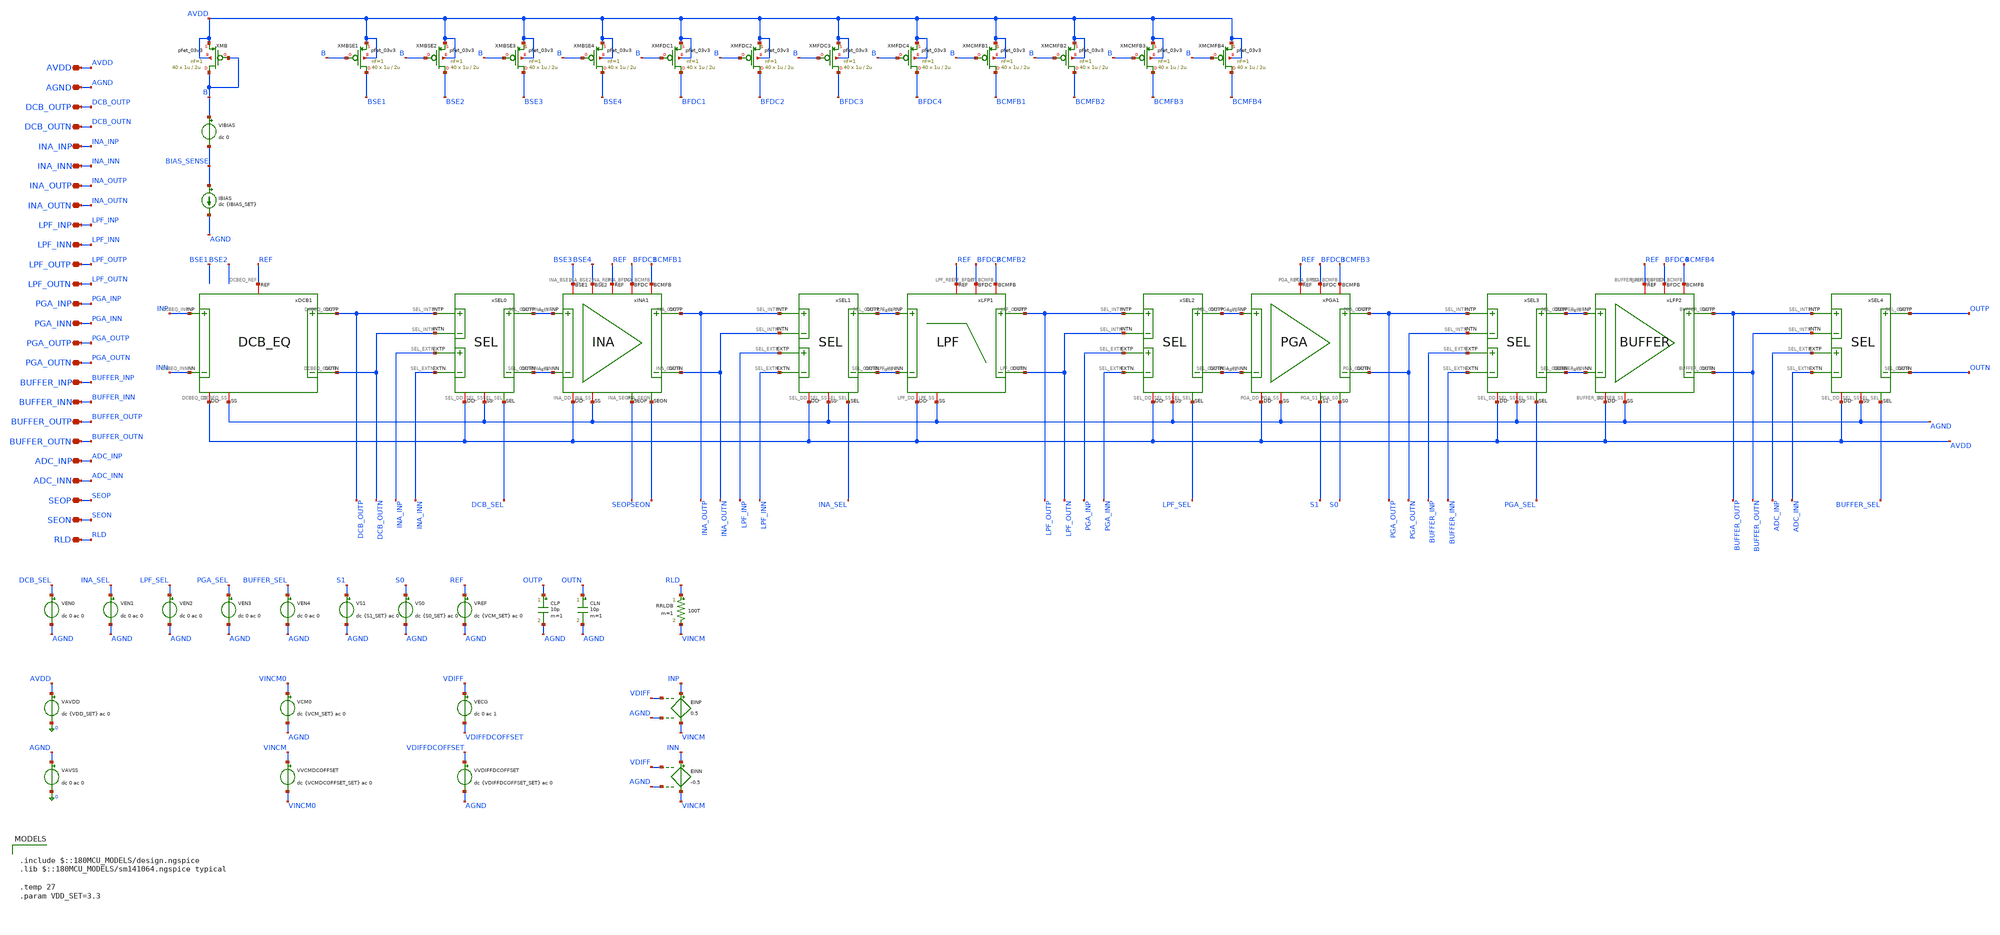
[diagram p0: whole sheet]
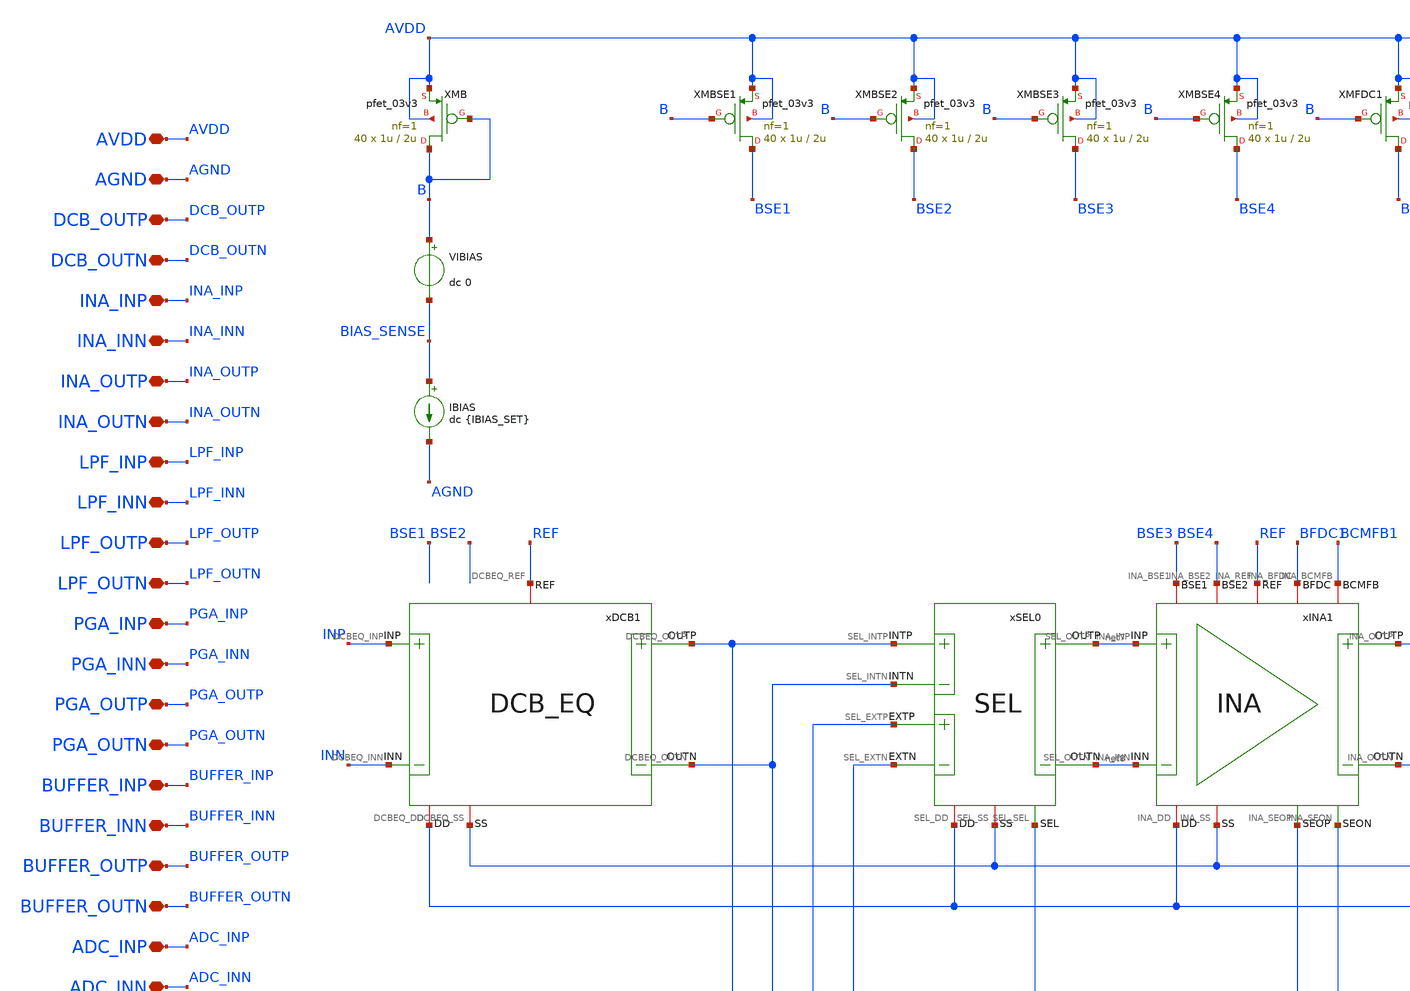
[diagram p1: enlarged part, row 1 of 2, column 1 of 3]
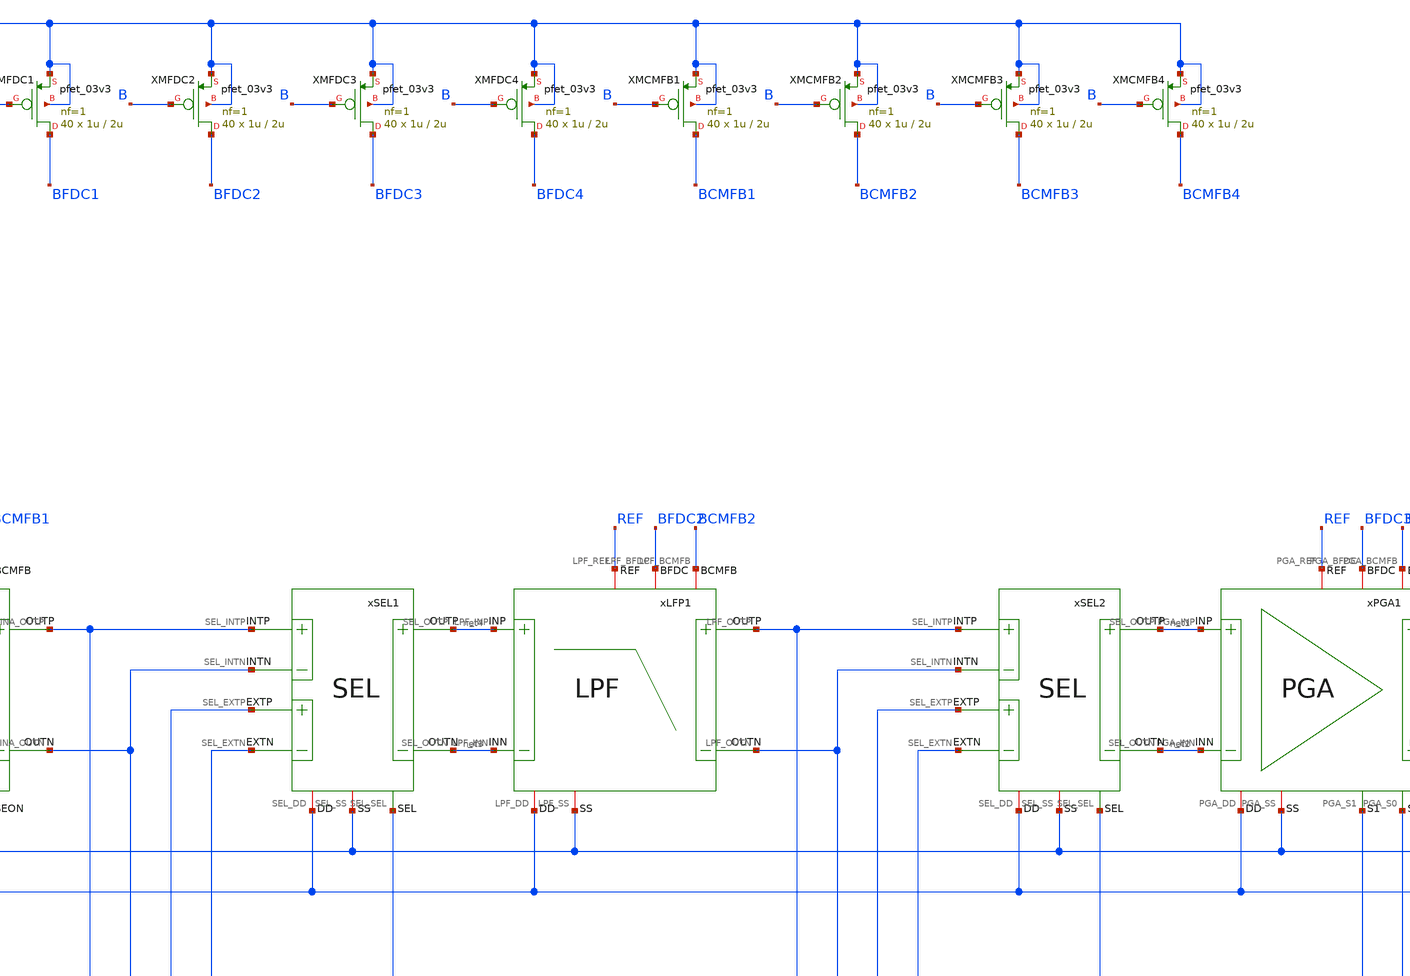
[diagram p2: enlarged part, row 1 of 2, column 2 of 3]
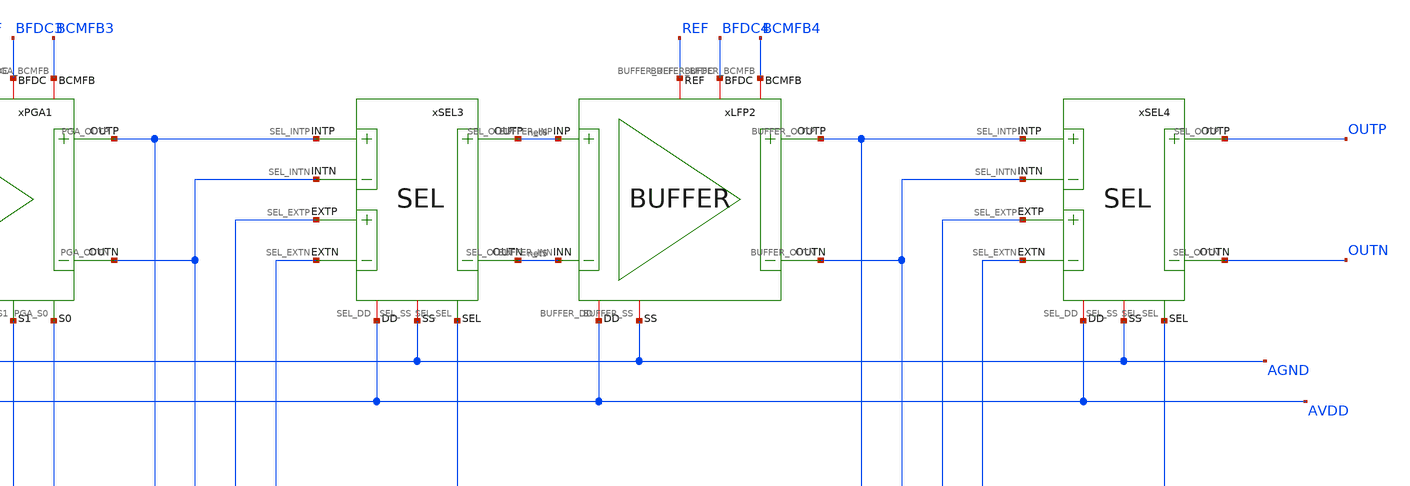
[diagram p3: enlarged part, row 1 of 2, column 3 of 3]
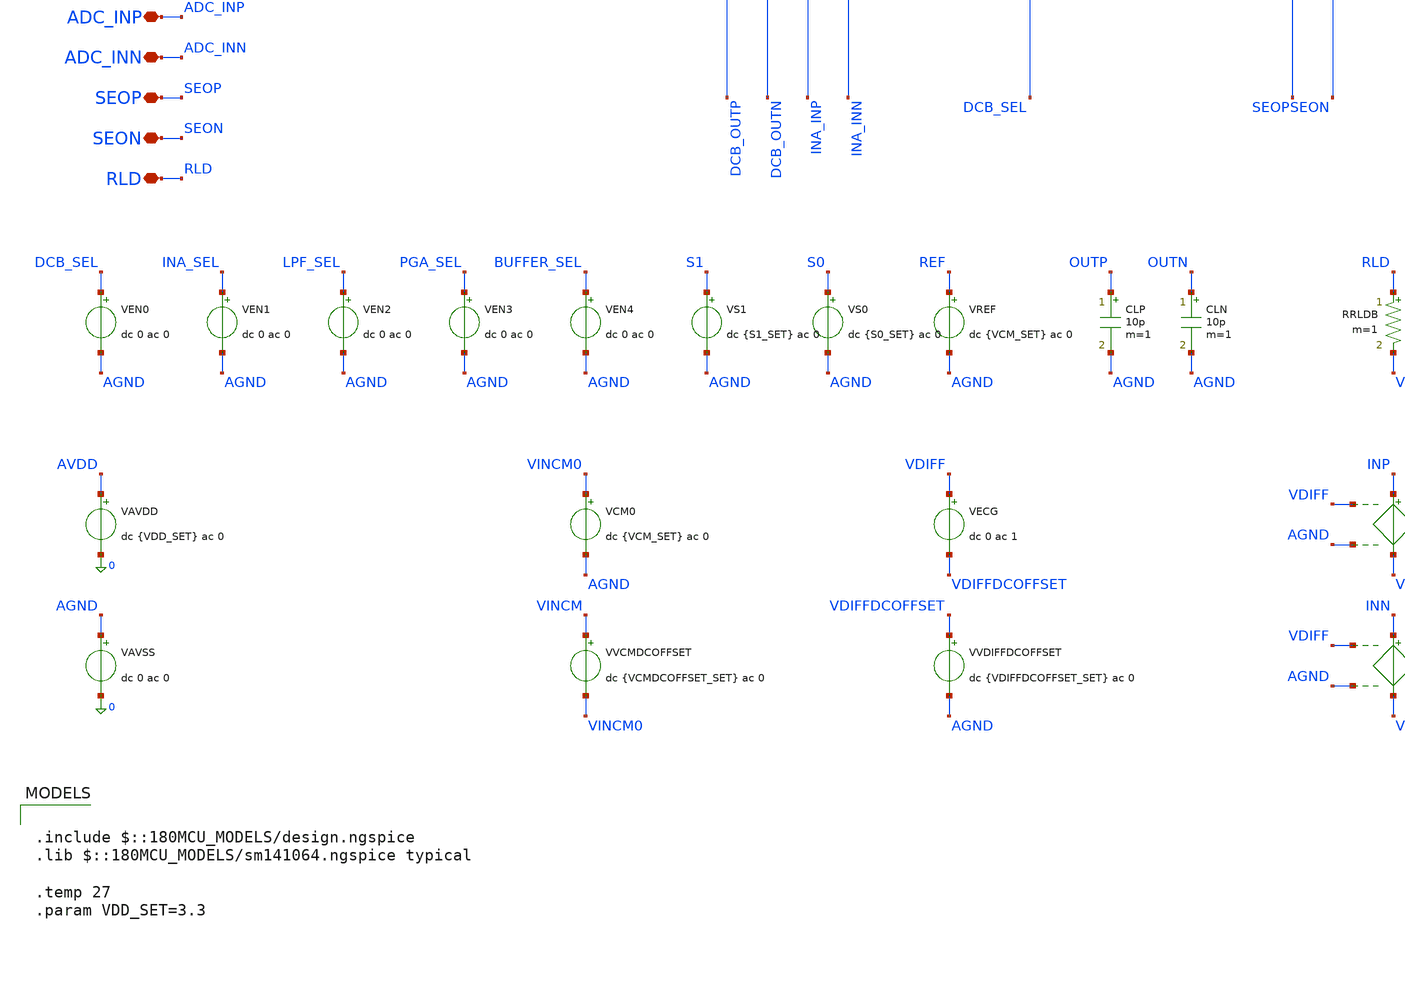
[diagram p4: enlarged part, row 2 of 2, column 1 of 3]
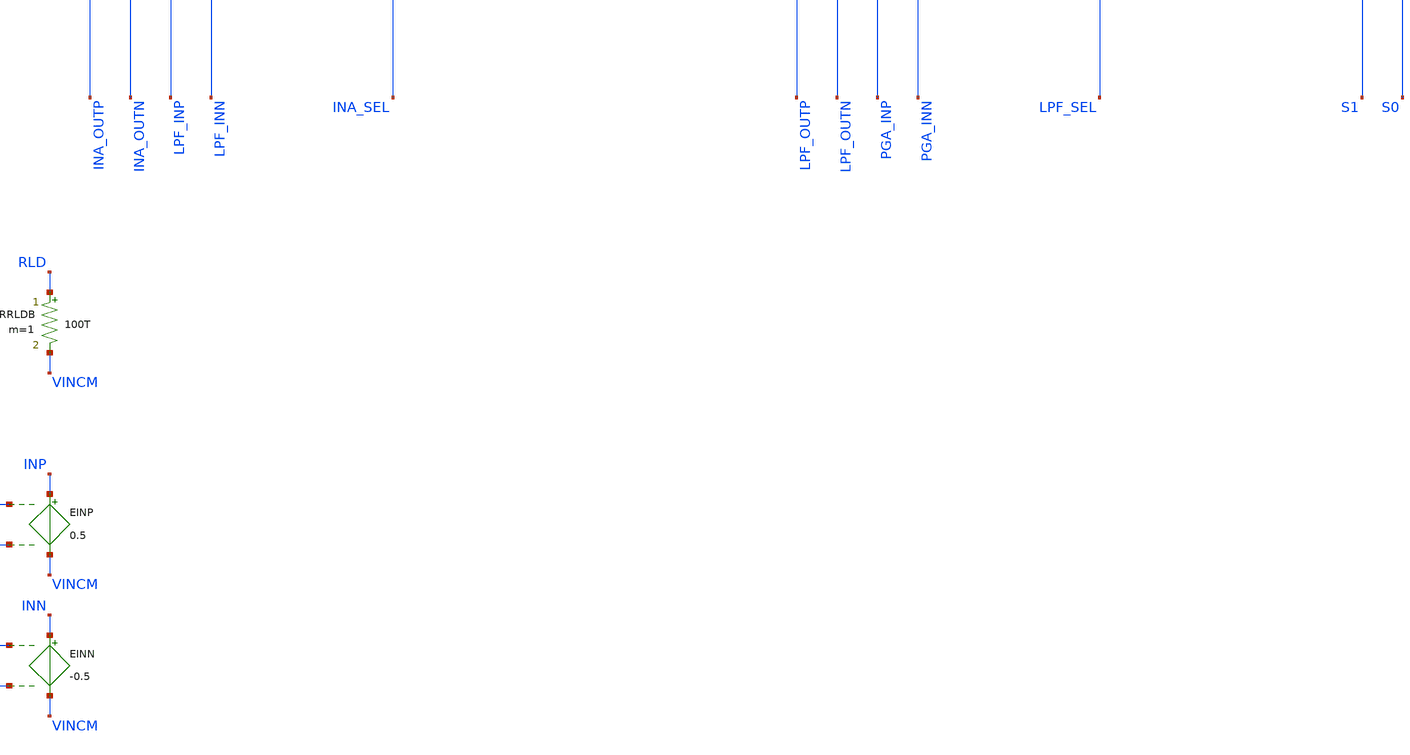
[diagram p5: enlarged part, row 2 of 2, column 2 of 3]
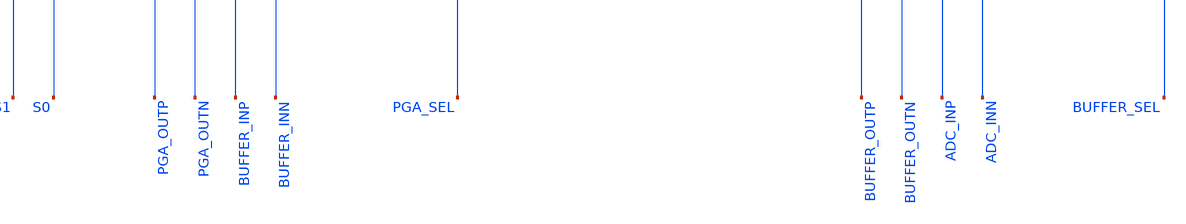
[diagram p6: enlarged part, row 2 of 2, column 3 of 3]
** sch_path: Design_Files/IC Design/Testbench/PATH/NOISE/PATH_TB_NOISE.sch
**.subckt PATH_TB_NOISE DCB_OUTP DCB_OUTN INA_INP INA_INN INA_OUTP INA_OUTN LPF_INP LPF_INN LPF_OUTP
*+ LPF_OUTN PGA_INP PGA_INN PGA_OUTP PGA_OUTN BUFFER_INP BUFFER_INN BUFFER_OUTP BUFFER_OUTN ADC_INP ADC_INN
*+ AVDD AGND SEOP SEON RLD
*.iopin DCB_OUTP
*.iopin DCB_OUTN
*.iopin INA_INP
*.iopin INA_INN
*.iopin INA_OUTP
*.iopin INA_OUTN
*.iopin LPF_INP
*.iopin LPF_INN
*.iopin LPF_OUTP
*.iopin LPF_OUTN
*.iopin PGA_INP
*.iopin PGA_INN
*.iopin PGA_OUTP
*.iopin PGA_OUTN
*.iopin BUFFER_INP
*.iopin BUFFER_INN
*.iopin BUFFER_OUTP
*.iopin BUFFER_OUTN
*.iopin ADC_INP
*.iopin ADC_INN
*.iopin AVDD
*.iopin AGND
*.iopin SEOP
*.iopin SEON
*.iopin RLD
CLP OUTP AGND 10p m=1
CLN OUTN AGND 10p m=1
VIBIAS B BIAS_SENSE dc 0
.save i(vibias)
IBIAS BIAS_SENSE AGND dc {IBIAS_SET}
VREF REF AGND dc {VCM_SET} ac 0
xLFP1 AVDD AGND net4 net3 LPF_OUTN BFDC2 LPF_OUTP BCMFB2 REF LPF
xPGA1 AVDD AGND net1 net2 PGA_OUTN BFDC3 PGA_OUTP BCMFB3 REF S1 S0 PGA
xSEL1 AVDD AGND INA_OUTP INA_OUTN net3 net4 LPF_INP LPF_INN INA_SEL SEL
xINA1 AVDD AGND net7 net8 INA_OUTN BFDC1 INA_OUTP BCMFB1 REF SEON SEOP BSE3 BSE4 INA
xSEL2 AVDD AGND LPF_OUTP LPF_OUTN net2 net1 PGA_INP PGA_INN LPF_SEL SEL
xSEL3 AVDD AGND PGA_OUTP PGA_OUTN net5 net6 BUFFER_INP BUFFER_INN PGA_SEL SEL
xSEL4 AVDD AGND BUFFER_OUTP BUFFER_OUTN OUTN OUTP ADC_INP ADC_INN BUFFER_SEL SEL
xLFP2 AVDD AGND net6 net5 BUFFER_OUTN BFDC4 BUFFER_OUTP BCMFB4 REF BUFFER
VEN1 INA_SEL AGND dc 0 ac 0
.save i(ven1)
VS0 S0 AGND dc {S0_SET} ac 0
VS1 S1 AGND dc {S1_SET} ac 0
xSEL0 AVDD AGND DCB_OUTP DCB_OUTN net8 net7 INA_INP INA_INN DCB_SEL SEL
VEN2 LPF_SEL AGND dc 0 ac 0
.save i(ven2)
VEN3 PGA_SEL AGND dc 0 ac 0
.save i(ven3)
VEN4 BUFFER_SEL AGND dc 0 ac 0
.save i(ven4)
VEN0 DCB_SEL AGND dc 0 ac 0
.save i(ven0)
xDCB1 AVDD AGND INP INN DCB_OUTP DCB_OUTN REF DCB_EQ
VAVDD AVDD 0 dc {VDD_SET} ac 0
.save i(vavdd)
VAVSS AGND 0 dc 0 ac 0
.save i(vavss)
VCM0 VINCM0 AGND dc {VCM_SET} ac 0
VVCMDCOFFSET VINCM VINCM0 dc {VCMDCOFFSET_SET} ac 0
VECG VDIFF VDIFFDCOFFSET dc 0 ac 1
VVDIFFDCOFFSET VDIFFDCOFFSET AGND dc {VDIFFDCOFFSET_SET} ac 0
EINP INP VINCM VDIFF AGND 0.5
EINN INN VINCM VDIFF AGND -0.5
RRLDB RLD VINCM 100T m=1
XMB B B AVDD AVDD pfet_03v3 L=2u W=1u nf=1 ad='int((nf+1)/2) * W/nf * 0.18u' as='int((nf+2)/2) * W/nf * 0.18u'
+ pd='2*int((nf+1)/2) * (W/nf + 0.18u)' ps='2*int((nf+2)/2) * (W/nf + 0.18u)' nrd='0.18u / W' nrs='0.18u / W'
+ sa=0 sb=0 sd=0 m=40
XMBSE3 BSE3 B AVDD AVDD pfet_03v3 L=2u W=1u nf=1 ad='int((nf+1)/2) * W/nf * 0.18u' as='int((nf+2)/2) * W/nf * 0.18u'
+ pd='2*int((nf+1)/2) * (W/nf + 0.18u)' ps='2*int((nf+2)/2) * (W/nf + 0.18u)' nrd='0.18u / W' nrs='0.18u / W'
+ sa=0 sb=0 sd=0 m=40
XMBSE4 BSE4 B AVDD AVDD pfet_03v3 L=2u W=1u nf=1 ad='int((nf+1)/2) * W/nf * 0.18u' as='int((nf+2)/2) * W/nf * 0.18u'
+ pd='2*int((nf+1)/2) * (W/nf + 0.18u)' ps='2*int((nf+2)/2) * (W/nf + 0.18u)' nrd='0.18u / W' nrs='0.18u / W'
+ sa=0 sb=0 sd=0 m=40
XMFDC1 BFDC1 B AVDD AVDD pfet_03v3 L=2u W=1u nf=1 ad='int((nf+1)/2) * W/nf * 0.18u' as='int((nf+2)/2) * W/nf * 0.18u'
+ pd='2*int((nf+1)/2) * (W/nf + 0.18u)' ps='2*int((nf+2)/2) * (W/nf + 0.18u)' nrd='0.18u / W' nrs='0.18u / W'
+ sa=0 sb=0 sd=0 m=40
XMFDC2 BFDC2 B AVDD AVDD pfet_03v3 L=2u W=1u nf=1 ad='int((nf+1)/2) * W/nf * 0.18u' as='int((nf+2)/2) * W/nf * 0.18u'
+ pd='2*int((nf+1)/2) * (W/nf + 0.18u)' ps='2*int((nf+2)/2) * (W/nf + 0.18u)' nrd='0.18u / W' nrs='0.18u / W'
+ sa=0 sb=0 sd=0 m=40
XMFDC3 BFDC3 B AVDD AVDD pfet_03v3 L=2u W=1u nf=1 ad='int((nf+1)/2) * W/nf * 0.18u' as='int((nf+2)/2) * W/nf * 0.18u'
+ pd='2*int((nf+1)/2) * (W/nf + 0.18u)' ps='2*int((nf+2)/2) * (W/nf + 0.18u)' nrd='0.18u / W' nrs='0.18u / W'
+ sa=0 sb=0 sd=0 m=40
XMFDC4 BFDC4 B AVDD AVDD pfet_03v3 L=2u W=1u nf=1 ad='int((nf+1)/2) * W/nf * 0.18u' as='int((nf+2)/2) * W/nf * 0.18u'
+ pd='2*int((nf+1)/2) * (W/nf + 0.18u)' ps='2*int((nf+2)/2) * (W/nf + 0.18u)' nrd='0.18u / W' nrs='0.18u / W'
+ sa=0 sb=0 sd=0 m=40
XMCMFB1 BCMFB1 B AVDD AVDD pfet_03v3 L=2u W=1u nf=1 ad='int((nf+1)/2) * W/nf * 0.18u' as='int((nf+2)/2) * W/nf * 0.18u'
+ pd='2*int((nf+1)/2) * (W/nf + 0.18u)' ps='2*int((nf+2)/2) * (W/nf + 0.18u)' nrd='0.18u / W' nrs='0.18u / W'
+ sa=0 sb=0 sd=0 m=40
XMCMFB2 BCMFB2 B AVDD AVDD pfet_03v3 L=2u W=1u nf=1 ad='int((nf+1)/2) * W/nf * 0.18u' as='int((nf+2)/2) * W/nf * 0.18u'
+ pd='2*int((nf+1)/2) * (W/nf + 0.18u)' ps='2*int((nf+2)/2) * (W/nf + 0.18u)' nrd='0.18u / W' nrs='0.18u / W'
+ sa=0 sb=0 sd=0 m=40
XMCMFB3 BCMFB3 B AVDD AVDD pfet_03v3 L=2u W=1u nf=1 ad='int((nf+1)/2) * W/nf * 0.18u' as='int((nf+2)/2) * W/nf * 0.18u'
+ pd='2*int((nf+1)/2) * (W/nf + 0.18u)' ps='2*int((nf+2)/2) * (W/nf + 0.18u)' nrd='0.18u / W' nrs='0.18u / W'
+ sa=0 sb=0 sd=0 m=40
XMCMFB4 BCMFB4 B AVDD AVDD pfet_03v3 L=2u W=1u nf=1 ad='int((nf+1)/2) * W/nf * 0.18u' as='int((nf+2)/2) * W/nf * 0.18u'
+ pd='2*int((nf+1)/2) * (W/nf + 0.18u)' ps='2*int((nf+2)/2) * (W/nf + 0.18u)' nrd='0.18u / W' nrs='0.18u / W'
+ sa=0 sb=0 sd=0 m=40
XMBSE1 BSE1 B AVDD AVDD pfet_03v3 L=2u W=1u nf=1 ad='int((nf+1)/2) * W/nf * 0.18u' as='int((nf+2)/2) * W/nf * 0.18u'
+ pd='2*int((nf+1)/2) * (W/nf + 0.18u)' ps='2*int((nf+2)/2) * (W/nf + 0.18u)' nrd='0.18u / W' nrs='0.18u / W'
+ sa=0 sb=0 sd=0 m=40
XMBSE2 BSE2 B AVDD AVDD pfet_03v3 L=2u W=1u nf=1 ad='int((nf+1)/2) * W/nf * 0.18u' as='int((nf+2)/2) * W/nf * 0.18u'
+ pd='2*int((nf+1)/2) * (W/nf + 0.18u)' ps='2*int((nf+2)/2) * (W/nf + 0.18u)' nrd='0.18u / W' nrs='0.18u / W'
+ sa=0 sb=0 sd=0 m=40
**** begin user architecture code

.include $::180MCU_MODELS/design.ngspice
.lib $::180MCU_MODELS/sm141064.ngspice typical

.temp 27
.param VDD_SET=3.3



.param VCM_SET={VDD_SET/2}

.param VCMDCOFFSET_SET=0
.param VDIFFDCOFFSET_SET=0

.param IBIAS_SET=40u

.param S1_SET=3.3
.param S0_SET=3.3

.options sparse
.options method=gear

.options reltol=1e-3
.options abstol=1e-12
.options vntol=1u
.options chgtol=1e-14

.options itl1=2000
.options itl2=1000
.options itl4=2000

.options gmin=1e-12
.options rshunt=100T

.nodeset v(B)=2.3

.nodeset v(INP)={VCM_SET}
.nodeset v(INN)={VCM_SET}

.nodeset v(OUTP)={VCM_SET}
.nodeset v(OUTN)={VCM_SET}

.nodeset v(RLD)={VCM_SET}

.save all





.control

destroy all

set noaskquit
set wr_singlescale
unset wr_vecnames
set appendwrite

unset sqrnoise

option numdgt=15
option sparse

shell mkdir -p
+ /foss/designs/ECG_Acquisition_IC/Measurement_Results/IC_Simulation/PATH/NOM.Result_txt

shell rm -f
+ /foss/designs/ECG_Acquisition_IC/Measurement_Results/IC_Simulation/PATH/NOM.Result_txt/NOM.noise_diff.txt


* Differential noise: PGA G2 and G16
foreach gaincfg 0 1

    if $gaincfg = 0
        alterparam S1_SET=0
        alterparam S0_SET=0
    else
        alterparam S1_SET=3.3
        alterparam S0_SET=3.3
    end

    reset
    save all

    alter @VECG[ACMAG]=1
    alter @VECG[ACPHASE]=0

    alter @VCM0[ACMAG]=0
    alter @VCM0[ACPHASE]=0

    alter @VAVDD[ACMAG]=0
    alter @VAVDD[ACPHASE]=0

    alter @VAVSS[ACMAG]=0
    alter @VAVSS[ACPHASE]=0

    op

    noise v(OUTP,OUTN) VECG dec 300 0.01 1k

    * noise leaves the one-row integrated plot active
    * previous plot contains the noise-density spectrum
    setplot previous
    setscale frequency

    if $gaincfg = 0
        let noise_pga_gain=frequency*0+2
    else
        let noise_pga_gain=frequency*0+16
    end

    let noise_out_density=onoise_spectrum
    let noise_in_density=inoise_spectrum

    wrdata
+ /foss/designs/ECG_Acquisition_IC/Measurement_Results/IC_Simulation/PATH/NOM.Result_txt/NOM.noise_diff.txt noise_pga_gain noise_out_density noise_in_density

    destroy all

end


* Last simulated setting is PGA G16

quit
.endc


**** end user architecture code
**.ends

* expanding   symbol:  ECG_Acquisition_IC/Design_Files/IC Design/Schematic/LPF/LPF.sym # of pins=9
** sym_path: Design_Files/IC Design/Schematic/LPF/LPF.sym
** sch_path: Design_Files/IC Design/Schematic/LPF/LPF.sch
.subckt LPF LPF_DD LPF_SS LPF_INP LPF_INN LPF_OUTN LPF_BFDC LPF_OUTP LPF_BCMFB LPF_REF
*.iopin LPF_DD
*.iopin LPF_SS
*.ipin LPF_INP
*.ipin LPF_INN
*.opin LPF_OUTP
*.iopin LPF_BFDC
*.opin LPF_OUTN
*.iopin LPF_BCMFB
*.iopin LPF_REF
RFBP net1 LPF_OUTN 3.7Meg m=1
xFDOTA1 LPF_DD LPF_SS net1 net2 LPF_OUTN LPF_BFDC LPF_OUTP LPF_BCMFB LPF_REF LPF_VOCM FD_OTA
RINN LPF_INN net2 3.7Meg m=1
RINP LPF_INP net1 3.7Meg m=1
RFBN net2 LPF_OUTP 3.7Meg m=1
CLPFP net1 LPF_OUTN 20p m=5
CLPFN net2 LPF_OUTP 20p m=5
.ends


* expanding   symbol:  ECG_Acquisition_IC/Design_Files/IC Design/Schematic/PGA/PGA.sym # of pins=11
** sym_path: Design_Files/IC Design/Schematic/PGA/PGA.sym
** sch_path: Design_Files/IC Design/Schematic/PGA/PGA.sch
.subckt PGA PGA_DD PGA_SS PGA_INP PGA_INN PGA_OUTN PGA_BFDC PGA_OUTP PGA_BCMFB PGA_REF PGA_S1 PGA_S0
*.iopin PGA_DD
*.iopin PGA_SS
*.ipin PGA_INP
*.ipin PGA_INN
*.opin PGA_OUTP
*.iopin PGA_BFDC
*.opin PGA_OUTN
*.iopin PGA_BCMFB
*.iopin PGA_REF
*.ipin PGA_S0
*.ipin PGA_S1
RFBP1 net2 net1 40k m=1
xFDOTA1 PGA_DD PGA_SS net2 net8 PGA_OUTN PGA_BFDC PGA_OUTP PGA_BCMFB PGA_REF PGA_VOCM FD_OTA
RFBP2 net1 net3 40k m=1
RFBP3 net3 net4 120k m=1
RFBP4 net4 PGA_OUTN 120k m=1
RINN PGA_INN net8 20k m=1
RINP PGA_INP net2 20k m=1
xTG1 PGA_DD PGA_SS net1 net3 S0B PGA_S0 TG
xTG3 PGA_DD PGA_SS net3 PGA_OUTN S1B PGA_S1 TG
xINV1 PGA_DD PGA_SS PGA_S0 S0B INV
xTG2 PGA_DD PGA_SS net3 net4 S0B PGA_S0 TG
RFBN1 net8 net5 40k m=1
RFBN2 net5 net6 40k m=1
RFBN3 net6 net7 120k m=1
RFBN4 net7 PGA_OUTP 120k m=1
xTG4 PGA_DD PGA_SS net5 net6 S0B PGA_S0 TG
xTG5 PGA_DD PGA_SS net6 net7 S0B PGA_S0 TG
xINV2 PGA_DD PGA_SS PGA_S1 S1B INV
xTG6 PGA_DD PGA_SS net6 PGA_OUTP S1B PGA_S1 TG
.ends


* expanding   symbol:  ECG_Acquisition_IC/Design_Files/IC Design/Schematic/SEL/SEL.sym # of pins=9
** sym_path: Design_Files/IC Design/Schematic/SEL/SEL.sym
** sch_path: Design_Files/IC Design/Schematic/SEL/SEL.sch
.subckt SEL SEL_DD SEL_SS SEL_INTP SEL_INTN SEL_OUTN SEL_OUTP SEL_EXTP SEL_EXTN SEL_SEL
*.iopin SEL_DD
*.iopin SEL_SS
*.ipin SEL_INTP
*.ipin SEL_INTN
*.iopin SEL_OUTP
*.iopin SEL_OUTN
*.ipin SEL_EXTP
*.ipin SEL_EXTN
*.ipin SEL_SEL
xINV1 SEL_DD SEL_SS SEL_SEL SELB INV
xTG1 SEL_DD SEL_SS SEL_EXTP SEL_OUTP SEL_SEL SELB TG
xTG2 SEL_DD SEL_SS SEL_INTP SEL_OUTP SELB SEL_SEL TG
xTG3 SEL_DD SEL_SS SEL_EXTN SEL_OUTN SEL_SEL SELB TG
xTG4 SEL_DD SEL_SS SEL_INTN SEL_OUTN SELB SEL_SEL TG
.ends


* expanding   symbol:  ECG_Acquisition_IC/Design_Files/IC Design/Schematic/INA/INA.sym # of pins=13
** sym_path: Design_Files/IC Design/Schematic/INA/INA.sym
** sch_path: Design_Files/IC Design/Schematic/INA/INA.sch
.subckt INA INA_DD INA_SS INA_INP INA_INN INA_OUTN INA_BFDC INA_OUTP INA_BCMFB INA_REF INA_SEON
+ INA_SEOP INA_BSE1 INA_BSE2
*.iopin INA_DD
*.iopin INA_SS
*.ipin INA_INP
*.ipin INA_INN
*.opin INA_OUTP
*.iopin INA_BFDC
*.opin INA_OUTN
*.iopin INA_BCMFB
*.iopin INA_REF
*.iopin INA_BSE1
*.iopin INA_SEON
*.iopin INA_SEOP
*.iopin INA_BSE2
RFDFBP INA_FDINP INA_OUTN 40k m=1
xFDOTA1 INA_DD INA_SS INA_FDINP INA_FDINN INA_OUTN INA_BFDC INA_OUTP INA_BCMFB INA_REF INA_VOCM
+ FD_OTA
xSEOTA1 INA_DD INA_SS INA_INP INA_SEFP INA_SEOP INA_BSE1 SE_OTA
xSEOTA2 INA_DD INA_SS INA_INN INA_SEFN INA_SEON INA_BSE2 SE_OTA
RFDFBN INA_FDINN INA_OUTP 40k m=1
RFDINP INA_SEOP INA_FDINP 10k m=1
RFDINN INA_SEON INA_FDINN 10k m=1
RSEFP INA_SEOP INA_SEFP 118k m=1
RSEFN INA_SEON INA_SEFN 118k m=1
RSEG INA_SEFP INA_SEFN 4k m=1
.ends


* expanding   symbol:  ECG_Acquisition_IC/Design_Files/IC Design/Schematic/BUFFER/BUFFER.sym # of
*+ pins=9
** sym_path: Design_Files/IC Design/Schematic/BUFFER/BUFFER.sym
** sch_path: Design_Files/IC Design/Schematic/BUFFER/BUFFER.sch
.subckt BUFFER BUFFER_DD BUFFER_SS BUFFER_INP BUFFER_INN BUFFER_OUTN BUFFER_BFDC BUFFER_OUTP
+ BUFFER_BCMFB BUFFER_REF
*.iopin BUFFER_DD
*.iopin BUFFER_SS
*.ipin BUFFER_INP
*.ipin BUFFER_INN
*.opin BUFFER_OUTP
*.iopin BUFFER_BFDC
*.opin BUFFER_OUTN
*.iopin BUFFER_BCMFB
*.iopin BUFFER_REF
RFBP net1 BUFFER_OUTN 20k m=1
xFDOTA1 BUFFER_DD BUFFER_SS net1 net2 BUFFER_OUTN BUFFER_BFDC BUFFER_OUTP BUFFER_BCMFB BUFFER_REF
+ BUFFER_VOCM FD_OTA
RINN BUFFER_INN net2 20k m=1
RINP BUFFER_INP net1 20k m=1
RFBN net2 BUFFER_OUTP 20k m=1
.ends


* expanding   symbol:  ECG_Acquisition_IC/Design_Files/IC Design/Schematic/DCB_EQ/DCB_EQ.sym # of
*+ pins=7
** sym_path: Design_Files/IC Design/Schematic/DCB_EQ/DCB_EQ.sym
** sch_path: Design_Files/IC Design/Schematic/DCB_EQ/DCB_EQ.sch
.subckt DCB_EQ DCBEQ_DD DCBEQ_SS DCBEQ_INP DCBEQ_INN DCBEQ_OUTP DCBEQ_OUTN DCBEQ_REF
*.iopin DCBEQ_DD
*.iopin DCBEQ_SS
*.ipin DCBEQ_INP
*.ipin DCBEQ_INN
*.opin DCBEQ_OUTP
*.opin DCBEQ_OUTN
*.iopin DCBEQ_REF
CBP DCBEQ_INP DCBEQ_OUTP 20p m=25
CBN DCBEQ_INN DCBEQ_OUTN 20p m=25
REQP DCBEQ_OUTP DCBEQ_REF 20G m=1
REQN DCBEQ_OUTN DCBEQ_REF 20G m=1
.ends


* expanding   symbol:  ECG_Acquisition_IC/Design_Files/IC Design/Schematic/FD_OTA/FDOTA/FD_OTA.sym #
*+ of pins=10
** sym_path: Design_Files/IC Design/Schematic/FD_OTA/FDOTA/FD_OTA.sym
** sch_path: Design_Files/IC Design/Schematic/FD_OTA/FDOTA/FD_OTA.sch
.subckt FD_OTA FDOTA_DD FDOTA_SS FDOTA_INP FDOTA_INN FDOTA_OUTN FDOTA_BFDC FDOTA_OUTP FDOTA_BCMFB
+ FDOTA_REF FDOTA_VOCM
*.iopin FDOTA_DD
*.iopin FDOTA_SS
*.ipin FDOTA_INP
*.ipin FDOTA_INN
*.opin FDOTA_OUTP
*.iopin FDOTA_BFDC
*.opin FDOTA_OUTN
*.iopin FDOTA_BCMFB
*.iopin FDOTA_REF
*.iopin FDOTA_VOCM
R1 FDOTA_OUTP FDOTA_VOCM 100k m=1
R2 FDOTA_VOCM FDOTA_OUTN 100k m=1
C1 FDOTA_OUTP FDOTA_VOCM 50f m=1
C2 FDOTA_VOCM FDOTA_OUTN 50f m=1
xFDC1 FDOTA_DD FDOTA_SS FDOTA_INP FDOTA_INN FDOTA_OUTN FDOTA_BFDC FDOTA_OUTP FDOTA_VCMFB FDC
xCMFB1 FDOTA_DD FDOTA_SS FDOTA_VOCM FDOTA_REF FDOTA_VCMFB FDOTA_BCMFB CMFB
.ends


* expanding   symbol:  ECG_Acquisition_IC/Design_Files/IC Design/Schematic/TG/TG.sym # of pins=6
** sym_path: Design_Files/IC Design/Schematic/TG/TG.sym
** sch_path: Design_Files/IC Design/Schematic/TG/TG.sch
.subckt TG TG_DD TG_SS TG_A TG_B TG_SEL TG_SELB
*.iopin TG_DD
*.iopin TG_SS
*.iopin TG_A
*.iopin TG_B
*.ipin TG_SEL
*.ipin TG_SELB
XMTGP TG_B TG_SELB TG_A TG_DD pfet_03v3 L=0.5u W=10u nf=1 ad='int((nf+1)/2) * W/nf * 0.18u' as='int((nf+2)/2) * W/nf * 0.18u'
+ pd='2*int((nf+1)/2) * (W/nf + 0.18u)' ps='2*int((nf+2)/2) * (W/nf + 0.18u)' nrd='0.18u / W' nrs='0.18u / W'
+ sa=0 sb=0 sd=0 m=1
XMTGN TG_A TG_SEL TG_B TG_SS nfet_03v3 L=0.5u W=5u nf=1 ad='int((nf+1)/2) * W/nf * 0.18u' as='int((nf+2)/2) * W/nf * 0.18u'
+ pd='2*int((nf+1)/2) * (W/nf + 0.18u)' ps='2*int((nf+2)/2) * (W/nf + 0.18u)' nrd='0.18u / W' nrs='0.18u / W'
+ sa=0 sb=0 sd=0 m=1
.ends


* expanding   symbol:  ECG_Acquisition_IC/Design_Files/IC Design/Schematic/INV/INV.sym # of pins=4
** sym_path: Design_Files/IC Design/Schematic/INV/INV.sym
** sch_path: Design_Files/IC Design/Schematic/INV/INV.sch
.subckt INV INV_DD INV_SS INV_IN INV_OUT
*.iopin INV_DD
*.iopin INV_SS
*.ipin INV_IN
*.opin INV_OUT
XMINVP INV_OUT INV_IN INV_DD INV_DD pfet_03v3 L=0.5u W=2u nf=1 ad='int((nf+1)/2) * W/nf * 0.18u' as='int((nf+2)/2) * W/nf * 0.18u'
+ pd='2*int((nf+1)/2) * (W/nf + 0.18u)' ps='2*int((nf+2)/2) * (W/nf + 0.18u)' nrd='0.18u / W' nrs='0.18u / W'
+ sa=0 sb=0 sd=0 m=1
XMINVN INV_OUT INV_IN INV_SS INV_SS nfet_03v3 L=0.5u W=1u nf=1 ad='int((nf+1)/2) * W/nf * 0.18u' as='int((nf+2)/2) * W/nf * 0.18u'
+ pd='2*int((nf+1)/2) * (W/nf + 0.18u)' ps='2*int((nf+2)/2) * (W/nf + 0.18u)' nrd='0.18u / W' nrs='0.18u / W'
+ sa=0 sb=0 sd=0 m=1
.ends


* expanding   symbol:  ECG_Acquisition_IC/Design_Files/IC Design/Schematic/SE_OTA/SE_OTA.sym # of
*+ pins=6
** sym_path: Design_Files/IC Design/Schematic/SE_OTA/SE_OTA.sym
** sch_path: Design_Files/IC Design/Schematic/SE_OTA/SE_OTA.sch
.subckt SE_OTA SEOTA_DD SEOTA_SS SEOTA_INP SEOTA_INN SEOTA_OUT SEOTA_B
*.iopin SEOTA_DD
*.iopin SEOTA_SS
*.ipin SEOTA_INP
*.ipin SEOTA_INN
*.opin SEOTA_OUT
*.iopin SEOTA_B
XM3 net4 net4 SEOTA_DD SEOTA_DD pfet_03v3 L=4u W=1u nf=1 ad='int((nf+1)/2) * W/nf * 0.18u' as='int((nf+2)/2) * W/nf * 0.18u'
+ pd='2*int((nf+1)/2) * (W/nf + 0.18u)' ps='2*int((nf+2)/2) * (W/nf + 0.18u)' nrd='0.18u / W' nrs='0.18u / W'
+ sa=0 sb=0 sd=0 m=60
XM7 SEOTA_OUT SEOTA_B SEOTA_SS SEOTA_SS nfet_03v3 L=0.5u W=1u nf=1 ad='int((nf+1)/2) * W/nf * 0.18u'
+ as='int((nf+2)/2) * W/nf * 0.18u' pd='2*int((nf+1)/2) * (W/nf + 0.18u)' ps='2*int((nf+2)/2) * (W/nf + 0.18u)'
+ nrd='0.18u / W' nrs='0.18u / W' sa=0 sb=0 sd=0 m=100
Rz net1 net2 3.8k m=1
XM5 net3 SEOTA_B SEOTA_SS SEOTA_SS nfet_03v3 L=2u W=1u nf=1 ad='int((nf+1)/2) * W/nf * 0.18u' as='int((nf+2)/2) * W/nf * 0.18u'
+ pd='2*int((nf+1)/2) * (W/nf + 0.18u)' ps='2*int((nf+2)/2) * (W/nf + 0.18u)' nrd='0.18u / W' nrs='0.18u / W'
+ sa=0 sb=0 sd=0 m=10
XM6 SEOTA_OUT net1 SEOTA_DD SEOTA_DD pfet_03v3 L=0.5u W=1u nf=1 ad='int((nf+1)/2) * W/nf * 0.18u' as='int((nf+2)/2) * W/nf * 0.18u'
+ pd='2*int((nf+1)/2) * (W/nf + 0.18u)' ps='2*int((nf+2)/2) * (W/nf + 0.18u)' nrd='0.18u / W' nrs='0.18u / W'
+ sa=0 sb=0 sd=0 m=400
XM8 SEOTA_B SEOTA_B SEOTA_SS SEOTA_SS nfet_03v3 L=2u W=1u nf=1 ad='int((nf+1)/2) * W/nf * 0.18u' as='int((nf+2)/2) * W/nf * 0.18u'
+ pd='2*int((nf+1)/2) * (W/nf + 0.18u)' ps='2*int((nf+2)/2) * (W/nf + 0.18u)' nrd='0.18u / W' nrs='0.18u / W'
+ sa=0 sb=0 sd=0 m=20
Cc net2 SEOTA_OUT 2p m=1
XM4 net1 net4 SEOTA_DD SEOTA_DD pfet_03v3 L=4u W=1u nf=1 ad='int((nf+1)/2) * W/nf * 0.18u' as='int((nf+2)/2) * W/nf * 0.18u'
+ pd='2*int((nf+1)/2) * (W/nf + 0.18u)' ps='2*int((nf+2)/2) * (W/nf + 0.18u)' nrd='0.18u / W' nrs='0.18u / W'
+ sa=0 sb=0 sd=0 m=60
XM1 net4 SEOTA_INN net3 SEOTA_SS nfet_03v3 L=4u W=1u nf=1 ad='int((nf+1)/2) * W/nf * 0.18u' as='int((nf+2)/2) * W/nf * 0.18u'
+ pd='2*int((nf+1)/2) * (W/nf + 0.18u)' ps='2*int((nf+2)/2) * (W/nf + 0.18u)' nrd='0.18u / W' nrs='0.18u / W'
+ sa=0 sb=0 sd=0 m=400
XM2 net1 SEOTA_INP net3 SEOTA_SS nfet_03v3 L=4u W=1u nf=1 ad='int((nf+1)/2) * W/nf * 0.18u' as='int((nf+2)/2) * W/nf * 0.18u'
+ pd='2*int((nf+1)/2) * (W/nf + 0.18u)' ps='2*int((nf+2)/2) * (W/nf + 0.18u)' nrd='0.18u / W' nrs='0.18u / W'
+ sa=0 sb=0 sd=0 m=400
.ends


* expanding   symbol:  ECG_Acquisition_IC/Design_Files/IC Design/Schematic/FD_OTA/FDC/FDC.sym # of
*+ pins=8
** sym_path: Design_Files/IC Design/Schematic/FD_OTA/FDC/FDC.sym
** sch_path: Design_Files/IC Design/Schematic/FD_OTA/FDC/FDC.sch
.subckt FDC FDC_DD FDC_SS FDC_INP FDC_INN FDC_OUTN FDC_B FDC_OUTP FDC_CMFB
*.iopin FDC_DD
*.iopin FDC_SS
*.ipin FDC_INP
*.ipin FDC_INN
*.opin FDC_OUTP
*.iopin FDC_B
*.opin FDC_OUTN
*.iopin FDC_CMFB
XM3 net4 FDC_CMFB FDC_DD FDC_DD pfet_03v3 L=2u W=1u nf=1 ad='int((nf+1)/2) * W/nf * 0.18u' as='int((nf+2)/2) * W/nf * 0.18u'
+ pd='2*int((nf+1)/2) * (W/nf + 0.18u)' ps='2*int((nf+2)/2) * (W/nf + 0.18u)' nrd='0.18u / W' nrs='0.18u / W'
+ sa=0 sb=0 sd=0 m=200
XM8 FDC_OUTP FDC_B FDC_SS FDC_SS nfet_03v3 L=0.5u W=1u nf=1 ad='int((nf+1)/2) * W/nf * 0.18u' as='int((nf+2)/2) * W/nf * 0.18u'
+ pd='2*int((nf+1)/2) * (W/nf + 0.18u)' ps='2*int((nf+2)/2) * (W/nf + 0.18u)' nrd='0.18u / W' nrs='0.18u / W'
+ sa=0 sb=0 sd=0 m=100
Rz net1 net2 3.5k m=1
XM5 net3 FDC_B FDC_SS FDC_SS nfet_03v3 L=2u W=1u nf=1 ad='int((nf+1)/2) * W/nf * 0.18u' as='int((nf+2)/2) * W/nf * 0.18u'
+ pd='2*int((nf+1)/2) * (W/nf + 0.18u)' ps='2*int((nf+2)/2) * (W/nf + 0.18u)' nrd='0.18u / W' nrs='0.18u / W'
+ sa=0 sb=0 sd=0 m=10
XM6 FDC_OUTP net1 FDC_DD FDC_DD pfet_03v3 L=0.5u W=1u nf=1 ad='int((nf+1)/2) * W/nf * 0.18u' as='int((nf+2)/2) * W/nf * 0.18u'
+ pd='2*int((nf+1)/2) * (W/nf + 0.18u)' ps='2*int((nf+2)/2) * (W/nf + 0.18u)' nrd='0.18u / W' nrs='0.18u / W'
+ sa=0 sb=0 sd=0 m=200
XM10 FDC_B FDC_B FDC_SS FDC_SS nfet_03v3 L=2u W=1u nf=1 ad='int((nf+1)/2) * W/nf * 0.18u' as='int((nf+2)/2) * W/nf * 0.18u'
+ pd='2*int((nf+1)/2) * (W/nf + 0.18u)' ps='2*int((nf+2)/2) * (W/nf + 0.18u)' nrd='0.18u / W' nrs='0.18u / W'
+ sa=0 sb=0 sd=0 m=20
Cc net2 FDC_OUTP 2.5p m=1
XM9 FDC_OUTN FDC_B FDC_SS FDC_SS nfet_03v3 L=0.5u W=1u nf=1 ad='int((nf+1)/2) * W/nf * 0.18u' as='int((nf+2)/2) * W/nf * 0.18u'
+ pd='2*int((nf+1)/2) * (W/nf + 0.18u)' ps='2*int((nf+2)/2) * (W/nf + 0.18u)' nrd='0.18u / W' nrs='0.18u / W'
+ sa=0 sb=0 sd=0 m=100
Rz1 net4 net5 3.5k m=1
XM7 FDC_OUTN net4 FDC_DD FDC_DD pfet_03v3 L=0.5u W=1u nf=1 ad='int((nf+1)/2) * W/nf * 0.18u' as='int((nf+2)/2) * W/nf * 0.18u'
+ pd='2*int((nf+1)/2) * (W/nf + 0.18u)' ps='2*int((nf+2)/2) * (W/nf + 0.18u)' nrd='0.18u / W' nrs='0.18u / W'
+ sa=0 sb=0 sd=0 m=200
Cc1 net5 FDC_OUTN 2.5p m=1
XM4 net1 FDC_CMFB FDC_DD FDC_DD pfet_03v3 L=2u W=1u nf=1 ad='int((nf+1)/2) * W/nf * 0.18u' as='int((nf+2)/2) * W/nf * 0.18u'
+ pd='2*int((nf+1)/2) * (W/nf + 0.18u)' ps='2*int((nf+2)/2) * (W/nf + 0.18u)' nrd='0.18u / W' nrs='0.18u / W'
+ sa=0 sb=0 sd=0 m=200
XM1 net4 FDC_INN net3 FDC_SS nfet_03v3 L=2u W=1u nf=1 ad='int((nf+1)/2) * W/nf * 0.18u' as='int((nf+2)/2) * W/nf * 0.18u'
+ pd='2*int((nf+1)/2) * (W/nf + 0.18u)' ps='2*int((nf+2)/2) * (W/nf + 0.18u)' nrd='0.18u / W' nrs='0.18u / W'
+ sa=0 sb=0 sd=0 m=200
XM2 net1 FDC_INP net3 FDC_SS nfet_03v3 L=2u W=1u nf=1 ad='int((nf+1)/2) * W/nf * 0.18u' as='int((nf+2)/2) * W/nf * 0.18u'
+ pd='2*int((nf+1)/2) * (W/nf + 0.18u)' ps='2*int((nf+2)/2) * (W/nf + 0.18u)' nrd='0.18u / W' nrs='0.18u / W'
+ sa=0 sb=0 sd=0 m=200
.ends


* expanding   symbol:  ECG_Acquisition_IC/Design_Files/IC Design/Schematic/FD_OTA/CMFB/CMFB.sym # of
*+ pins=6
** sym_path: Design_Files/IC Design/Schematic/FD_OTA/CMFB/CMFB.sym
** sch_path: Design_Files/IC Design/Schematic/FD_OTA/CMFB/CMFB.sch
.subckt CMFB CMFB_DD CMFB_SS CMFB_IN CMFB_REF CMFB_OUT CMFB_B
*.iopin CMFB_DD
*.iopin CMFB_SS
*.ipin CMFB_IN
*.ipin CMFB_REF
*.opin CMFB_OUT
*.iopin CMFB_B
XM4 CMFB_OUT CMFB_OUT CMFB_DD CMFB_DD pfet_03v3 L=0.5u W=1u nf=1 ad='int((nf+1)/2) * W/nf * 0.18u' as='int((nf+2)/2) * W/nf * 0.18u'
+ pd='2*int((nf+1)/2) * (W/nf + 0.18u)' ps='2*int((nf+2)/2) * (W/nf + 0.18u)' nrd='0.18u / W' nrs='0.18u / W'
+ sa=0 sb=0 sd=0 m=77
XM3 net2 net2 CMFB_DD CMFB_DD pfet_03v3 L=0.5u W=1u nf=1 ad='int((nf+1)/2) * W/nf * 0.18u' as='int((nf+2)/2) * W/nf * 0.18u'
+ pd='2*int((nf+1)/2) * (W/nf + 0.18u)' ps='2*int((nf+2)/2) * (W/nf + 0.18u)' nrd='0.18u / W' nrs='0.18u / W'
+ sa=0 sb=0 sd=0 m=77
XM1 net2 CMFB_REF net1 CMFB_SS nfet_03v3 L=0.5u W=1u nf=1 ad='int((nf+1)/2) * W/nf * 0.18u' as='int((nf+2)/2) * W/nf * 0.18u'
+ pd='2*int((nf+1)/2) * (W/nf + 0.18u)' ps='2*int((nf+2)/2) * (W/nf + 0.18u)' nrd='0.18u / W' nrs='0.18u / W'
+ sa=0 sb=0 sd=0 m=5
XM2 CMFB_OUT CMFB_IN net1 CMFB_SS nfet_03v3 L=0.5u W=1u nf=1 ad='int((nf+1)/2) * W/nf * 0.18u' as='int((nf+2)/2) * W/nf * 0.18u'
+ pd='2*int((nf+1)/2) * (W/nf + 0.18u)' ps='2*int((nf+2)/2) * (W/nf + 0.18u)' nrd='0.18u / W' nrs='0.18u / W'
+ sa=0 sb=0 sd=0 m=5
XM5 net1 CMFB_B CMFB_SS CMFB_SS nfet_03v3 L=2u W=1u nf=1 ad='int((nf+1)/2) * W/nf * 0.18u' as='int((nf+2)/2) * W/nf * 0.18u'
+ pd='2*int((nf+1)/2) * (W/nf + 0.18u)' ps='2*int((nf+2)/2) * (W/nf + 0.18u)' nrd='0.18u / W' nrs='0.18u / W'
+ sa=0 sb=0 sd=0 m=20
XM10 CMFB_B CMFB_B CMFB_SS CMFB_SS nfet_03v3 L=2u W=1u nf=1 ad='int((nf+1)/2) * W/nf * 0.18u' as='int((nf+2)/2) * W/nf * 0.18u'
+ pd='2*int((nf+1)/2) * (W/nf + 0.18u)' ps='2*int((nf+2)/2) * (W/nf + 0.18u)' nrd='0.18u / W' nrs='0.18u / W'
+ sa=0 sb=0 sd=0 m=20
.ends

.end
